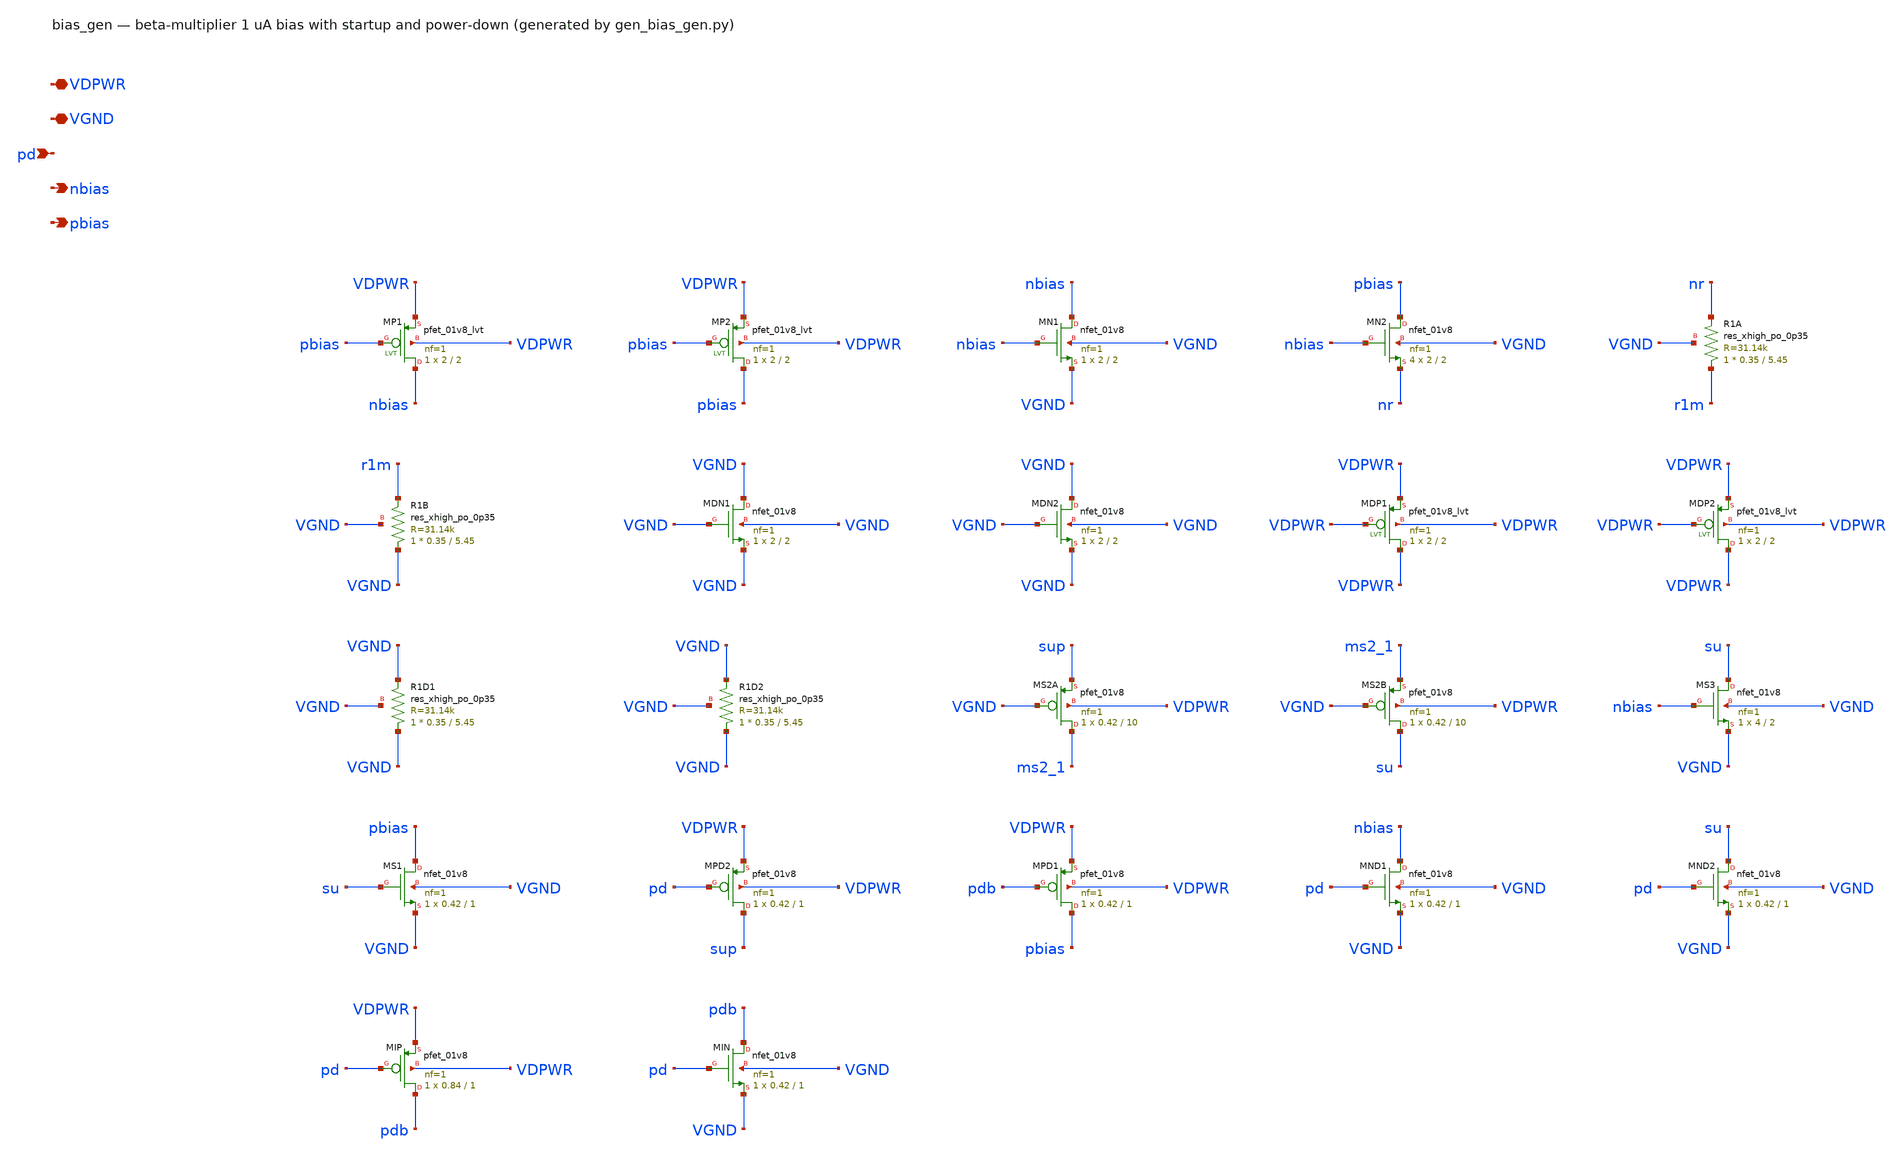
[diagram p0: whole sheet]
** sch_path: xschem/bias_gen.sch
**.subckt bias_gen VDPWR VGND pd nbias pbias
*.iopin VDPWR
*.iopin VGND
*.ipin pd
*.opin nbias
*.opin pbias
XMP1 nbias pbias VDPWR VDPWR sky130_fd_pr__pfet_01v8_lvt L=2 W=2 nf=1 ad='int((1 + 1)/2) * 2 / 1 * 0.29'
+ as='int((1 + 2)/2) * 2 / 1 * 0.29' pd='2*int((1 + 1)/2) * (2 / 1 + 0.29)' ps='2*int((1 + 2)/2) * (2 / 1 + 0.29)'
+ nrd='0.29 / 2 ' nrs='0.29 / 2 ' sa=0 sb=0 sd=0 mult=1 m=1
XMP2 pbias pbias VDPWR VDPWR sky130_fd_pr__pfet_01v8_lvt L=2 W=2 nf=1 ad='int((1 + 1)/2) * 2 / 1 * 0.29'
+ as='int((1 + 2)/2) * 2 / 1 * 0.29' pd='2*int((1 + 1)/2) * (2 / 1 + 0.29)' ps='2*int((1 + 2)/2) * (2 / 1 + 0.29)'
+ nrd='0.29 / 2 ' nrs='0.29 / 2 ' sa=0 sb=0 sd=0 mult=1 m=1
XMN1 nbias nbias VGND VGND sky130_fd_pr__nfet_01v8 L=2 W=2 nf=1 ad='int((1 + 1)/2) * 2 / 1 * 0.29' as='int((1 + 2)/2) * 2 / 1 * 0.29'
+ pd='2*int((1 + 1)/2) * (2 / 1 + 0.29)' ps='2*int((1 + 2)/2) * (2 / 1 + 0.29)' nrd='0.29 / 2 ' nrs='0.29 / 2 '
+ sa=0 sb=0 sd=0 mult=1 m=1
XMN2 pbias nbias nr VGND sky130_fd_pr__nfet_01v8 L=2 W=2 nf=1 ad='int((1 + 1)/2) * 2 / 1 * 0.29' as='int((1 + 2)/2) * 2 / 1 * 0.29'
+ pd='2*int((1 + 1)/2) * (2 / 1 + 0.29)' ps='2*int((1 + 2)/2) * (2 / 1 + 0.29)' nrd='0.29 / 2 ' nrs='0.29 / 2 '
+ sa=0 sb=0 sd=0 mult=4 m=4
XR1A r1m nr VGND sky130_fd_pr__res_xhigh_po_0p35 L=5.45 mult=1 m=1
XR1B VGND r1m VGND sky130_fd_pr__res_xhigh_po_0p35 L=5.45 mult=1 m=1
XMDN1 VGND VGND VGND VGND sky130_fd_pr__nfet_01v8 L=2 W=2 nf=1 ad='int((1 + 1)/2) * 2 / 1 * 0.29' as='int((1 + 2)/2) * 2 / 1 * 0.29'
+ pd='2*int((1 + 1)/2) * (2 / 1 + 0.29)' ps='2*int((1 + 2)/2) * (2 / 1 + 0.29)' nrd='0.29 / 2 ' nrs='0.29 / 2 '
+ sa=0 sb=0 sd=0 mult=1 m=1
XMDN2 VGND VGND VGND VGND sky130_fd_pr__nfet_01v8 L=2 W=2 nf=1 ad='int((1 + 1)/2) * 2 / 1 * 0.29' as='int((1 + 2)/2) * 2 / 1 * 0.29'
+ pd='2*int((1 + 1)/2) * (2 / 1 + 0.29)' ps='2*int((1 + 2)/2) * (2 / 1 + 0.29)' nrd='0.29 / 2 ' nrs='0.29 / 2 '
+ sa=0 sb=0 sd=0 mult=1 m=1
XMDP1 VDPWR VDPWR VDPWR VDPWR sky130_fd_pr__pfet_01v8_lvt L=2 W=2 nf=1 ad='int((1 + 1)/2) * 2 / 1 * 0.29'
+ as='int((1 + 2)/2) * 2 / 1 * 0.29' pd='2*int((1 + 1)/2) * (2 / 1 + 0.29)' ps='2*int((1 + 2)/2) * (2 / 1 + 0.29)'
+ nrd='0.29 / 2 ' nrs='0.29 / 2 ' sa=0 sb=0 sd=0 mult=1 m=1
XMDP2 VDPWR VDPWR VDPWR VDPWR sky130_fd_pr__pfet_01v8_lvt L=2 W=2 nf=1 ad='int((1 + 1)/2) * 2 / 1 * 0.29'
+ as='int((1 + 2)/2) * 2 / 1 * 0.29' pd='2*int((1 + 1)/2) * (2 / 1 + 0.29)' ps='2*int((1 + 2)/2) * (2 / 1 + 0.29)'
+ nrd='0.29 / 2 ' nrs='0.29 / 2 ' sa=0 sb=0 sd=0 mult=1 m=1
XR1D1 VGND VGND VGND sky130_fd_pr__res_xhigh_po_0p35 L=5.45 mult=1 m=1
XR1D2 VGND VGND VGND sky130_fd_pr__res_xhigh_po_0p35 L=5.45 mult=1 m=1
XMS2A ms2_1 VGND sup VDPWR sky130_fd_pr__pfet_01v8 L=10 W=0.42 nf=1 ad='int((nf+1)/2) * W/nf * 0.29'
+ as='int((nf+2)/2) * W/nf * 0.29' pd='2*int((nf+1)/2) * (W/nf + 0.29)' ps='2*int((nf+2)/2) * (W/nf + 0.29)'
+ nrd='0.29 / W' nrs='0.29 / W' sa=0 sb=0 sd=0 mult=1 m=1
XMS2B su VGND ms2_1 VDPWR sky130_fd_pr__pfet_01v8 L=10 W=0.42 nf=1 ad='int((nf+1)/2) * W/nf * 0.29' as='int((nf+2)/2) * W/nf * 0.29'
+ pd='2*int((nf+1)/2) * (W/nf + 0.29)' ps='2*int((nf+2)/2) * (W/nf + 0.29)' nrd='0.29 / W' nrs='0.29 / W'
+ sa=0 sb=0 sd=0 mult=1 m=1
XMS3 su nbias VGND VGND sky130_fd_pr__nfet_01v8 L=2 W=4 nf=1 ad='int((1 + 1)/2) * 4 / 1 * 0.29' as='int((1 + 2)/2) * 4 / 1 * 0.29'
+ pd='2*int((1 + 1)/2) * (4 / 1 + 0.29)' ps='2*int((1 + 2)/2) * (4 / 1 + 0.29)' nrd='0.29 / 4 ' nrs='0.29 / 4 '
+ sa=0 sb=0 sd=0 mult=1 m=1
XMS1 pbias su VGND VGND sky130_fd_pr__nfet_01v8 L=1 W=0.42 nf=1 ad='int((1 + 1)/2) * 0.42 / 1 * 0.29'
+ as='int((1 + 2)/2) * 0.42 / 1 * 0.29' pd='2*int((1 + 1)/2) * (0.42 / 1 + 0.29)' ps='2*int((1 + 2)/2) * (0.42 / 1 + 0.29)'
+ nrd='0.29 / 0.42 ' nrs='0.29 / 0.42 ' sa=0 sb=0 sd=0 mult=1 m=1
XMPD2 sup pd VDPWR VDPWR sky130_fd_pr__pfet_01v8 L=1 W=0.42 nf=1 ad='int((nf+1)/2) * W/nf * 0.29' as='int((nf+2)/2) * W/nf * 0.29'
+ pd='2*int((nf+1)/2) * (W/nf + 0.29)' ps='2*int((nf+2)/2) * (W/nf + 0.29)' nrd='0.29 / W' nrs='0.29 / W'
+ sa=0 sb=0 sd=0 mult=1 m=1
XMPD1 pbias pdb VDPWR VDPWR sky130_fd_pr__pfet_01v8 L=1 W=0.42 nf=1 ad='int((nf+1)/2) * W/nf * 0.29'
+ as='int((nf+2)/2) * W/nf * 0.29' pd='2*int((nf+1)/2) * (W/nf + 0.29)' ps='2*int((nf+2)/2) * (W/nf + 0.29)'
+ nrd='0.29 / W' nrs='0.29 / W' sa=0 sb=0 sd=0 mult=1 m=1
XMND1 nbias pd VGND VGND sky130_fd_pr__nfet_01v8 L=1 W=0.42 nf=1 ad='int((1 + 1)/2) * 0.42 / 1 * 0.29'
+ as='int((1 + 2)/2) * 0.42 / 1 * 0.29' pd='2*int((1 + 1)/2) * (0.42 / 1 + 0.29)' ps='2*int((1 + 2)/2) * (0.42 / 1 + 0.29)'
+ nrd='0.29 / 0.42 ' nrs='0.29 / 0.42 ' sa=0 sb=0 sd=0 mult=1 m=1
XMND2 su pd VGND VGND sky130_fd_pr__nfet_01v8 L=1 W=0.42 nf=1 ad='int((1 + 1)/2) * 0.42 / 1 * 0.29' as='int((1 + 2)/2) * 0.42 / 1 * 0.29'
+ pd='2*int((1 + 1)/2) * (0.42 / 1 + 0.29)' ps='2*int((1 + 2)/2) * (0.42 / 1 + 0.29)' nrd='0.29 / 0.42 '
+ nrs='0.29 / 0.42 ' sa=0 sb=0 sd=0 mult=1 m=1
XMIP pdb pd VDPWR VDPWR sky130_fd_pr__pfet_01v8 L=1 W=0.84 nf=1 ad='int((nf+1)/2) * W/nf * 0.29' as='int((nf+2)/2) * W/nf * 0.29'
+ pd='2*int((nf+1)/2) * (W/nf + 0.29)' ps='2*int((nf+2)/2) * (W/nf + 0.29)' nrd='0.29 / W' nrs='0.29 / W'
+ sa=0 sb=0 sd=0 mult=1 m=1
XMIN pdb pd VGND VGND sky130_fd_pr__nfet_01v8 L=1 W=0.42 nf=1 ad='int((1 + 1)/2) * 0.42 / 1 * 0.29' as='int((1 + 2)/2) * 0.42 / 1 * 0.29'
+ pd='2*int((1 + 1)/2) * (0.42 / 1 + 0.29)' ps='2*int((1 + 2)/2) * (0.42 / 1 + 0.29)' nrd='0.29 / 0.42 '
+ nrs='0.29 / 0.42 ' sa=0 sb=0 sd=0 mult=1 m=1
**.ends
.end
